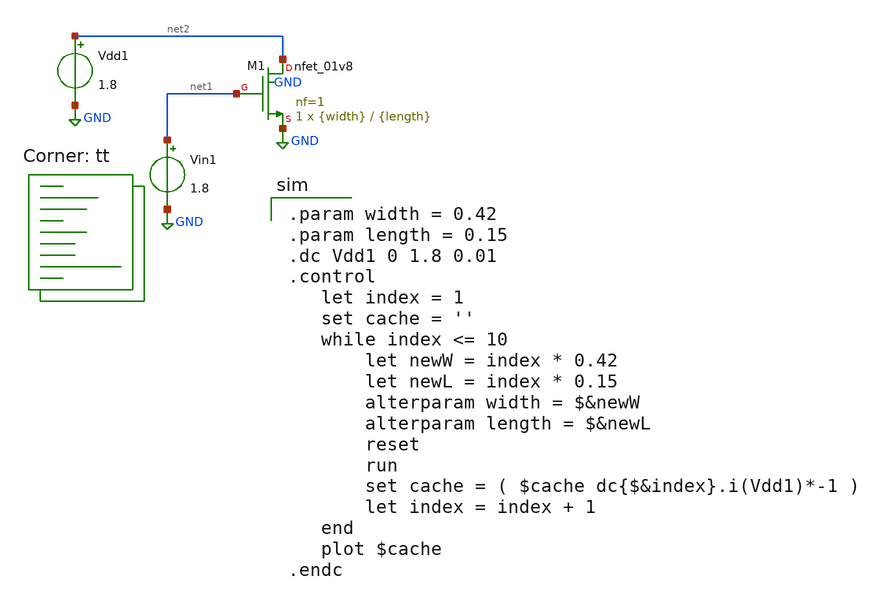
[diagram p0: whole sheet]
** sch_path: tutorial_2/tutorial_2_1c.sch
**.subckt tutorial_2_1c
XM1 net2 net1 GND GND sky130_fd_pr__nfet_01v8 L={length} W={width} nf=1 ad='int((nf+1)/2) * W/nf * 0.29'
+ as='int((nf+2)/2) * W/nf * 0.29' pd='2*int((nf+1)/2) * (W/nf + 0.29)' ps='2*int((nf+2)/2) * (W/nf + 0.29)'
+ nrd='0.29 / W' nrs='0.29 / W' sa=0 sb=0 sd=0 mult=1 m=1
Vdd1 net2 GND 1.8
Vin1 net1 GND 1.8
**** begin user architecture code

.param width = 0.42
.param length = 0.15
.dc Vdd1 0 1.8 0.01
.control
   let index = 1
   set cache = ''
   while index <= 10
       let newW = index * 0.42
       let newL = index * 0.15
       alterparam width = $&newW
       alterparam length = $&newL
       reset
       run
       set cache = ( $cache dc{$&index}.i(Vdd1)*-1 )
       let index = index + 1
   end
   plot $cache
.endc

.lib $::SKYWATER_MODELS/sky130.lib.spice tt
**** end user architecture code
**.ends
.GLOBAL GND
.end
